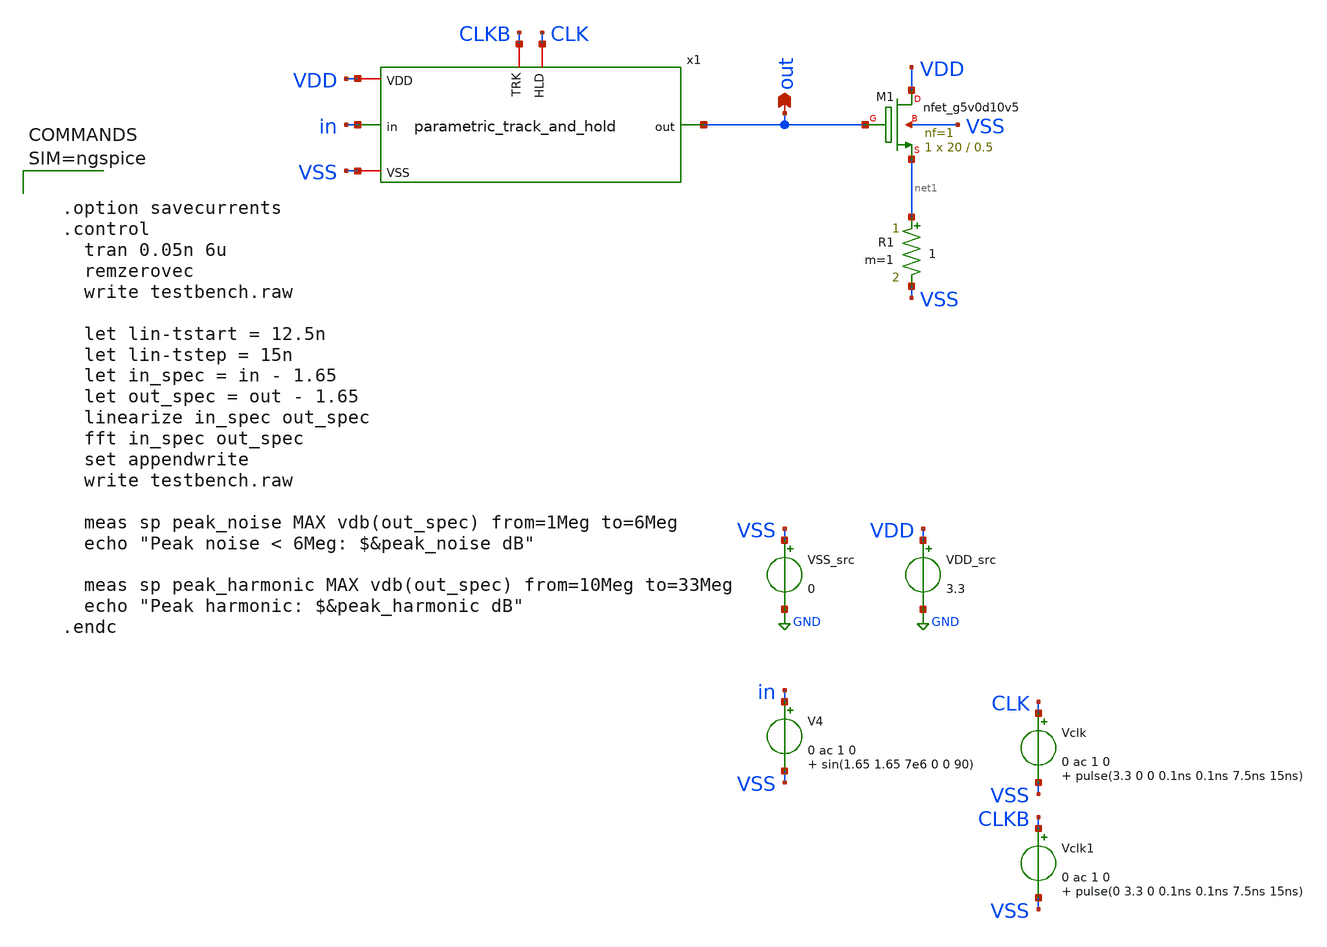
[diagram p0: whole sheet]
** sch_path: xschem/testbench.sch
**.subckt testbench out
*.opin out
VDD_src VDD GND 3.3
VSS_src VSS GND 0
V4 in VSS 0 ac 1 0 sin(1.65 1.65 7e6 0 0 90)
XM1 VDD out net1 VSS sky130_fd_pr__nfet_g5v0d10v5 L=0.5 W=20 nf=1 ad='int((nf+1)/2) * W/nf * 0.29' as='int((nf+2)/2) * W/nf * 0.29'
+ pd='2*int((nf+1)/2) * (W/nf + 0.29)' ps='2*int((nf+2)/2) * (W/nf + 0.29)' nrd='0.29 / W' nrs='0.29 / W'
+ sa=0 sb=0 sd=0 mult=1 m=1
R1 net1 VSS 1 m=1
Vclk CLK VSS 0 ac 1 0 pulse(3.3 0 0 0.1ns 0.1ns 7.5ns 15ns)
Vclk1 CLKB VSS 0 ac 1 0 pulse(0 3.3 0 0.1ns 0.1ns 7.5ns 15ns)
x1 CLK CLKB VDD VSS out in parametric_track_and_hold WT=1 PFT=1.21 PF=2 WS=5 WB=5 CB=18
**** begin user architecture code

** opencircuitdesign pdks install
.lib $::SKYWATER_MODELS/sky130.lib.spice tt





  .option savecurrents
  .control
    tran 0.05n 6u
    remzerovec
    write testbench.raw

    let lin-tstart = 12.5n
    let lin-tstep = 15n
    let in_spec = in - 1.65
    let out_spec = out - 1.65
    linearize in_spec out_spec
    fft in_spec out_spec
    set appendwrite
    write testbench.raw

    meas sp peak_noise MAX vdb(out_spec) from=1Meg to=6Meg
    echo "Peak noise < 6Meg: $&peak_noise dB"

    meas sp peak_harmonic MAX vdb(out_spec) from=10Meg to=33Meg
    echo "Peak harmonic: $&peak_harmonic dB"
  .endc



**** end user architecture code
**.ends
.GLOBAL GND
.end
